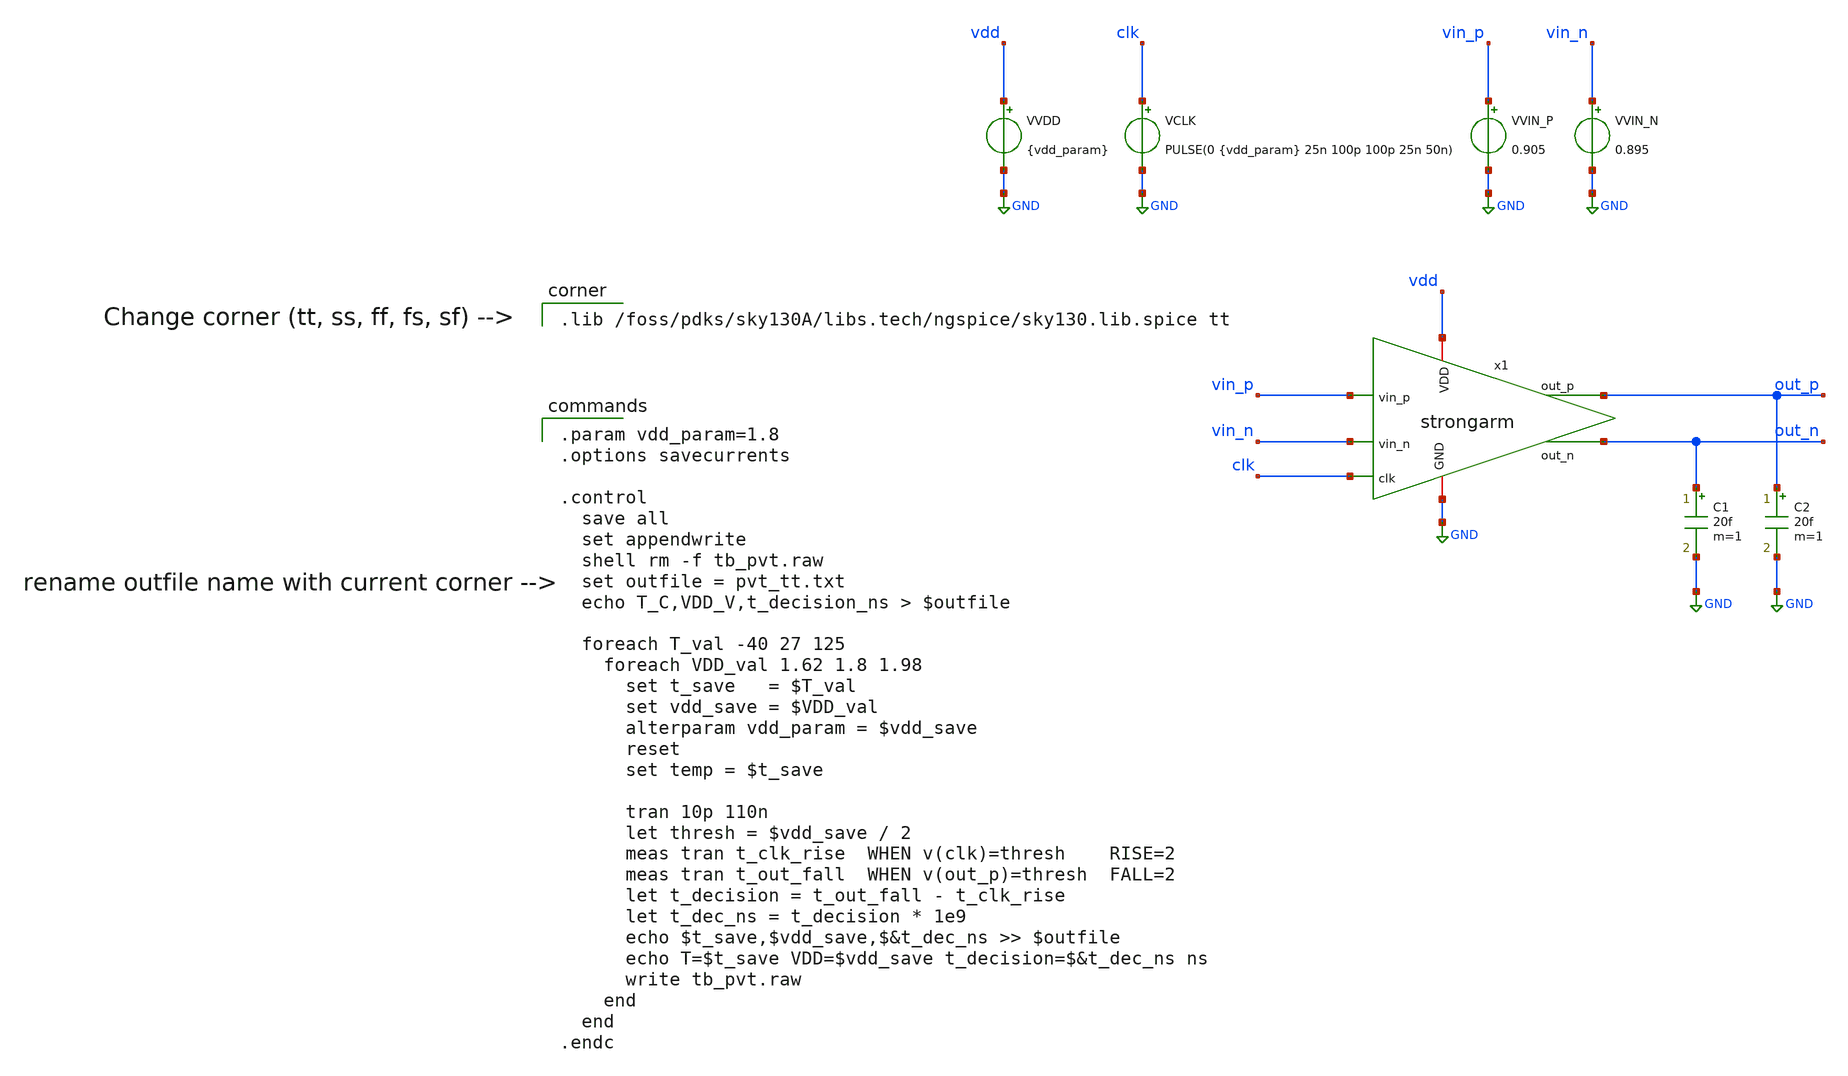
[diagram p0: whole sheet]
** sch_path: 01_xschem_ngspice/soluzioni/lab03/xschem/tb_pvt.sch
**.subckt tb_pvt
x1 vdd out_p out_n vin_p vin_n clk GND strongarm
VVDD vdd GND {vdd_param}
VCLK clk GND PULSE(0 {vdd_param} 25n 100p 100p 25n 50n)
VVIN_P vin_p GND 0.905
VVIN_N vin_n GND 0.895
C1 out_n GND 20f m=1
C2 out_p GND 20f m=1
**** begin user architecture code

.lib /foss/pdks/sky130A/libs.tech/ngspice/sky130.lib.spice tt


.param vdd_param=1.8
.options savecurrents

.control
  save all
  set appendwrite
  shell rm -f tb_pvt.raw
  set outfile = pvt_tt.txt
  echo T_C,VDD_V,t_decision_ns > $outfile

  foreach T_val -40 27 125
    foreach VDD_val 1.62 1.8 1.98
      set t_save   = $T_val
      set vdd_save = $VDD_val
      alterparam vdd_param = $vdd_save
      reset
      set temp = $t_save

      tran 10p 110n
      let thresh = $vdd_save / 2
      meas tran t_clk_rise  WHEN v(clk)=thresh    RISE=2
      meas tran t_out_fall  WHEN v(out_p)=thresh  FALL=2
      let t_decision = t_out_fall - t_clk_rise
      let t_dec_ns = t_decision * 1e9
      echo $t_save,$vdd_save,$&t_dec_ns >> $outfile
      echo T=$t_save VDD=$vdd_save t_decision=$&t_dec_ns ns
      write tb_pvt.raw
    end
  end
.endc

**** end user architecture code
**.ends
.GLOBAL GND
.end
